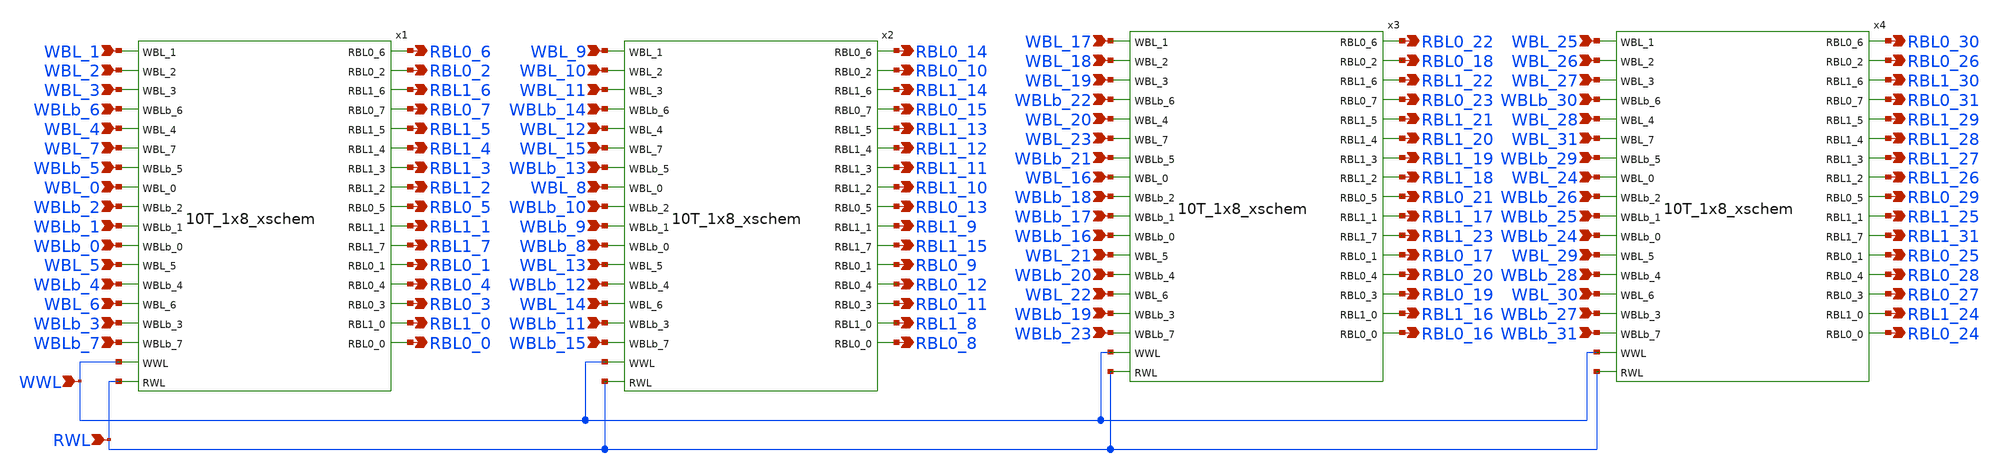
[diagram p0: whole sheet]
** sch_path: custom/xschem/10T_1x32_xschem.sch
**.subckt 10T_1x32_xschem WBL_1 RBL0_6 WBL_2 WBL_3 WBLb_6 WBL_4 WBL_7 WBLb_5 WBL_0 WBLb_2 WBLb_1
*+ WBLb_0 WBL_5 WBLb_4 WBL_6 WBLb_3 WBLb_7 WWL RWL RBL0_2 RBL1_6 RBL0_7 RBL1_5 RBL1_4 RBL1_3 RBL1_2 RBL0_5
*+ RBL1_1 RBL1_7 RBL0_1 RBL0_4 RBL0_3 RBL1_0 RBL0_0 RBL0_8 RBL0_9 RBL0_10 RBL0_11 RBL0_12 RBL0_13 RBL0_14
*+ RBL0_15 RBL1_8 RBL1_9 RBL1_10 RBL1_11 RBL1_12 RBL1_13 RBL1_14 RBL1_15 WBL_8 WBL_9 WBL_10 WBL_11 WBL_12
*+ WBL_13 WBL_14 WBL_15 WBLb_8 WBLb_9 WBLb_10 WBLb_11 WBLb_12 WBLb_13 WBLb_14 WBLb_15 RBL0_16 RBL0_18 RBL0_19
*+ RBL0_20 RBL0_21 RBL0_22 RBL0_17 RBL0_23 RBL1_16 RBL1_17 RBL1_18 RBL1_19 RBL1_20 RBL1_21 RBL1_22 RBL1_23
*+ WBL_16 WBL_17 WBL_18 WBL_19 WBL_20 WBL_21 WBL_22 WBL_23 WBLb_16 WBLb_17 WBLb_18 WBLb_19 WBLb_20 WBLb_21
*+ WBLb_22 WBLb_23 WBL_24 WBL_25 WBL_26 WBL_27 WBL_28 WBL_29 WBL_30 WBL_31 WBLb_24 WBLb_25 WBLb_26 WBLb_27
*+ WBLb_28 WBLb_29 WBLb_30 WBLb_31 RBL0_24 RBL0_26 RBL0_25 RBL0_27 RBL0_28 RBL0_29 RBL0_30 RBL0_31 RBL1_24
*+ RBL1_25 RBL1_26 RBL1_27 RBL1_28 RBL1_29 RBL1_30 RBL1_31
*.ipin WBL_1
*.opin RBL0_6
*.ipin WBL_2
*.ipin WBL_3
*.ipin WBLb_6
*.ipin WBL_4
*.ipin WBL_7
*.ipin WBLb_5
*.ipin WBL_0
*.ipin WBLb_2
*.ipin WBLb_1
*.ipin WBLb_0
*.ipin WBL_5
*.ipin WBLb_4
*.ipin WBL_6
*.ipin WBLb_3
*.ipin WBLb_7
*.ipin WWL
*.ipin RWL
*.opin RBL0_2
*.opin RBL1_6
*.opin RBL0_7
*.opin RBL1_5
*.opin RBL1_4
*.opin RBL1_3
*.opin RBL1_2
*.opin RBL0_5
*.opin RBL1_1
*.opin RBL1_7
*.opin RBL0_1
*.opin RBL0_4
*.opin RBL0_3
*.opin RBL1_0
*.opin RBL0_0
*.opin RBL0_8
*.opin RBL0_9
*.opin RBL0_10
*.opin RBL0_11
*.opin RBL0_12
*.opin RBL0_13
*.opin RBL0_14
*.opin RBL0_15
*.opin RBL1_8
*.opin RBL1_9
*.opin RBL1_10
*.opin RBL1_11
*.opin RBL1_12
*.opin RBL1_13
*.opin RBL1_14
*.opin RBL1_15
*.ipin WBL_8
*.ipin WBL_9
*.ipin WBL_10
*.ipin WBL_11
*.ipin WBL_12
*.ipin WBL_13
*.ipin WBL_14
*.ipin WBL_15
*.ipin WBLb_8
*.ipin WBLb_9
*.ipin WBLb_10
*.ipin WBLb_11
*.ipin WBLb_12
*.ipin WBLb_13
*.ipin WBLb_14
*.ipin WBLb_15
*.opin RBL0_16
*.opin RBL0_18
*.opin RBL0_19
*.opin RBL0_20
*.opin RBL0_21
*.opin RBL0_22
*.opin RBL0_17
*.opin RBL0_23
*.opin RBL1_16
*.opin RBL1_17
*.opin RBL1_18
*.opin RBL1_19
*.opin RBL1_20
*.opin RBL1_21
*.opin RBL1_22
*.opin RBL1_23
*.ipin WBL_16
*.ipin WBL_17
*.ipin WBL_18
*.ipin WBL_19
*.ipin WBL_20
*.ipin WBL_21
*.ipin WBL_22
*.ipin WBL_23
*.ipin WBLb_16
*.ipin WBLb_17
*.ipin WBLb_18
*.ipin WBLb_19
*.ipin WBLb_20
*.ipin WBLb_21
*.ipin WBLb_22
*.ipin WBLb_23
*.ipin WBL_24
*.ipin WBL_25
*.ipin WBL_26
*.ipin WBL_27
*.ipin WBL_28
*.ipin WBL_29
*.ipin WBL_30
*.ipin WBL_31
*.ipin WBLb_24
*.ipin WBLb_25
*.ipin WBLb_26
*.ipin WBLb_27
*.ipin WBLb_28
*.ipin WBLb_29
*.ipin WBLb_30
*.ipin WBLb_31
*.opin RBL0_24
*.opin RBL0_26
*.opin RBL0_25
*.opin RBL0_27
*.opin RBL0_28
*.opin RBL0_29
*.opin RBL0_30
*.opin RBL0_31
*.opin RBL1_24
*.opin RBL1_25
*.opin RBL1_26
*.opin RBL1_27
*.opin RBL1_28
*.opin RBL1_29
*.opin RBL1_30
*.opin RBL1_31
x1 WBL_1 WBL_2 WBL_3 WBLb_6 WBL_4 WBL_7 WBLb_5 WBL_0 WBLb_2 WBLb_1 WBLb_0 WBL_5 WBLb_4 WBL_6 WBLb_3
+ WBLb_7 WWL RWL RBL0_6 RBL0_2 RBL1_6 RBL0_7 RBL1_5 RBL1_4 RBL1_3 RBL1_2 RBL0_5 RBL1_1 RBL1_7 RBL0_1 RBL0_4
+ RBL0_3 RBL1_0 RBL0_0 VDD GND 10T_1x8_xschem
x2 WBL_9 WBL_10 WBL_11 WBLb_14 WBL_12 WBL_15 WBLb_13 WBL_8 WBLb_10 WBLb_9 WBLb_8 WBL_13 WBLb_12
+ WBL_14 WBLb_11 WBLb_15 WWL RWL RBL0_14 RBL0_10 RBL1_14 RBL0_15 RBL1_13 RBL1_12 RBL1_11 RBL1_10 RBL0_13
+ RBL1_9 RBL1_15 RBL0_9 RBL0_12 RBL0_11 RBL1_8 RBL0_8 VDD GND 10T_1x8_xschem
x3 WBL_17 WBL_18 WBL_19 WBLb_22 WBL_20 WBL_23 WBLb_21 WBL_16 WBLb_18 WBLb_17 WBLb_16 WBL_21 WBLb_20
+ WBL_22 WBLb_19 WBLb_23 WWL RWL RBL0_22 RBL0_18 RBL1_22 RBL0_23 RBL1_21 RBL1_20 RBL1_19 RBL1_18 RBL0_21
+ RBL1_17 RBL1_23 RBL0_17 RBL0_20 RBL0_19 RBL1_16 RBL0_16 VDD GND 10T_1x8_xschem
x4 WBL_25 WBL_26 WBL_27 WBLb_30 WBL_28 WBL_31 WBLb_29 WBL_24 WBLb_26 WBLb_25 WBLb_24 WBL_29 WBLb_28
+ WBL_30 WBLb_27 WBLb_31 WWL RWL RBL0_30 RBL0_26 RBL1_30 RBL0_31 RBL1_29 RBL1_28 RBL1_27 RBL1_26 RBL0_29
+ RBL1_25 RBL1_31 RBL0_25 RBL0_28 RBL0_27 RBL1_24 RBL0_24 VDD GND 10T_1x8_xschem
**.ends

* expanding   symbol:  10T_1x8_xschem.sym # of pins=34
** sym_path: custom/xschem/10T_1x8_xschem.sym
** sch_path: custom/xschem/10T_1x8_xschem.sch
.subckt 10T_1x8_xschem WBL_1 WBL_2 WBL_3 WBLb_6 WBL_4 WBL_7 WBLb_5 WBL_0 WBLb_2 WBLb_1 WBLb_0 WBL_5
+ WBLb_4 WBL_6 WBLb_3 WBLb_7 WWL RWL RBL0_6 RBL0_2 RBL1_6 RBL0_7 RBL1_5 RBL1_4 RBL1_3 RBL1_2 RBL0_5 RBL1_1
+ RBL1_7 RBL0_1 RBL0_4 RBL0_3 RBL1_0 RBL0_0 VDD GND
*.ipin WBLb_0
*.opin RBL0_0
*.ipin WBL_0
*.ipin WBLb_1
*.ipin WBL_1
*.ipin WBLb_2
*.ipin WBL_2
*.ipin WBLb_3
*.ipin WBL_3
*.ipin WBLb_4
*.ipin WBL_4
*.ipin WBL_5
*.ipin WBLb_5
*.ipin WBL_6
*.ipin WBLb_6
*.ipin WBLb_7
*.ipin WBL_7
*.opin RBL1_0
*.opin RBL0_1
*.opin RBL1_1
*.opin RBL0_2
*.opin RBL1_2
*.opin RBL0_3
*.opin RBL1_3
*.opin RBL0_4
*.opin RBL1_4
*.opin RBL0_5
*.opin RBL1_5
*.opin RBL0_6
*.opin RBL1_6
*.opin RBL0_7
*.opin RBL1_7
*.ipin WWL
*.ipin RWL
x1 WWL WBL_0 RBL0_0 RBL1_0 WBLb_0 RWL RWL VDD GND 10T_toy_xschem
x2 WWL WBL_1 RBL0_1 RBL1_1 WBLb_1 RWL RWL VDD GND 10T_toy_xschem
x3 WWL WBL_2 RBL0_2 RBL1_2 WBLb_2 RWL RWL VDD GND 10T_toy_xschem
x4 WWL WBL_3 RBL0_3 RBL1_3 WBLb_3 RWL RWL VDD GND 10T_toy_xschem
x5 WWL WBL_4 RBL0_4 RBL1_4 WBLb_4 RWL RWL VDD GND 10T_toy_xschem
x6 WWL WBL_5 RBL0_5 RBL1_5 WBLb_5 RWL RWL VDD GND 10T_toy_xschem
x7 WWL WBL_6 RBL0_6 RBL1_6 WBLb_6 RWL RWL VDD GND 10T_toy_xschem
x8 WWL WBL_7 RBL0_7 RBL1_7 WBLb_7 RWL RWL VDD GND 10T_toy_xschem
.ends


* expanding   symbol:  10T_toy_xschem.sym # of pins=7
** sym_path: custom/xschem/10T_toy_xschem.sym
** sch_path: custom/xschem/10T_toy_xschem.sch
.subckt 10T_toy_xschem WWL WBL RBL0 RBL1 WBLb RWL0 RWL1 VDD GND
*.ipin WWL
*.ipin RWL0
*.ipin RWL1
*.ipin WBL
*.ipin WBLb
*.opin RBL0
*.opin RBL1
x1 net1 net2 VDD GND INVX1
x2 net2 net1 VDD GND INVX1
XM1 net2 WWL WBL GND sky130_fd_pr__nfet_01v8 L=0.15 W=0.14 nf=1 ad='int((nf+1)/2) * W/nf * 0.29' as='int((nf+2)/2) * W/nf * 0.29'
+ pd='2*int((nf+1)/2) * (W/nf + 0.29)' ps='2*int((nf+2)/2) * (W/nf + 0.29)' nrd='0.29 / W' nrs='0.29 / W'
+ sa=0 sb=0 sd=0 mult=1 m=1
XM2 WBLb WWL net1 GND sky130_fd_pr__nfet_01v8 L=0.15 W=0.14 nf=1 ad='int((nf+1)/2) * W/nf * 0.29' as='int((nf+2)/2) * W/nf * 0.29'
+ pd='2*int((nf+1)/2) * (W/nf + 0.29)' ps='2*int((nf+2)/2) * (W/nf + 0.29)' nrd='0.29 / W' nrs='0.29 / W'
+ sa=0 sb=0 sd=0 mult=1 m=1
XM3 net3 net2 GND GND sky130_fd_pr__nfet_01v8 L=0.15 W=0.14 nf=1 ad='int((nf+1)/2) * W/nf * 0.29' as='int((nf+2)/2) * W/nf * 0.29'
+ pd='2*int((nf+1)/2) * (W/nf + 0.29)' ps='2*int((nf+2)/2) * (W/nf + 0.29)' nrd='0.29 / W' nrs='0.29 / W'
+ sa=0 sb=0 sd=0 mult=1 m=1
XM4 RBL0 RWL0 net3 GND sky130_fd_pr__nfet_01v8 L=0.15 W=0.21 nf=1 ad='int((nf+1)/2) * W/nf * 0.29' as='int((nf+2)/2) * W/nf * 0.29'
+ pd='2*int((nf+1)/2) * (W/nf + 0.29)' ps='2*int((nf+2)/2) * (W/nf + 0.29)' nrd='0.29 / W' nrs='0.29 / W'
+ sa=0 sb=0 sd=0 mult=1 m=1
XM5 net4 net1 GND GND sky130_fd_pr__nfet_01v8 L=0.15 W=0.14 nf=1 ad='int((nf+1)/2) * W/nf * 0.29' as='int((nf+2)/2) * W/nf * 0.29'
+ pd='2*int((nf+1)/2) * (W/nf + 0.29)' ps='2*int((nf+2)/2) * (W/nf + 0.29)' nrd='0.29 / W' nrs='0.29 / W'
+ sa=0 sb=0 sd=0 mult=1 m=1
XM6 RBL1 RWL1 net4 GND sky130_fd_pr__nfet_01v8 L=0.15 W=0.21 nf=1 ad='int((nf+1)/2) * W/nf * 0.29' as='int((nf+2)/2) * W/nf * 0.29'
+ pd='2*int((nf+1)/2) * (W/nf + 0.29)' ps='2*int((nf+2)/2) * (W/nf + 0.29)' nrd='0.29 / W' nrs='0.29 / W'
+ sa=0 sb=0 sd=0 mult=1 m=1
.ends


* expanding   symbol:  INVX1.sym # of pins=2
** sym_path: custom/xschem/INVX1.sym
** sch_path: custom/xschem/INVX1.sch
.subckt INVX1 Y A VDD GND
*.ipin A
*.opin Y
XM1 Y A GND GND sky130_fd_pr__nfet_01v8 L=0.15 W=0.21 nf=1 ad='int((nf+1)/2) * W/nf * 0.29' as='int((nf+2)/2) * W/nf * 0.29'
+ pd='2*int((nf+1)/2) * (W/nf + 0.29)' ps='2*int((nf+2)/2) * (W/nf + 0.29)' nrd='0.29 / W' nrs='0.29 / W'
+ sa=0 sb=0 sd=0 mult=1 m=1
XM2 Y A VDD VDD sky130_fd_pr__pfet_01v8 L=0.15 W=0.14 nf=1 ad='int((nf+1)/2) * W/nf * 0.29' as='int((nf+2)/2) * W/nf * 0.29'
+ pd='2*int((nf+1)/2) * (W/nf + 0.29)' ps='2*int((nf+2)/2) * (W/nf + 0.29)' nrd='0.29 / W' nrs='0.29 / W'
+ sa=0 sb=0 sd=0 mult=1 m=1
.ends

.end
